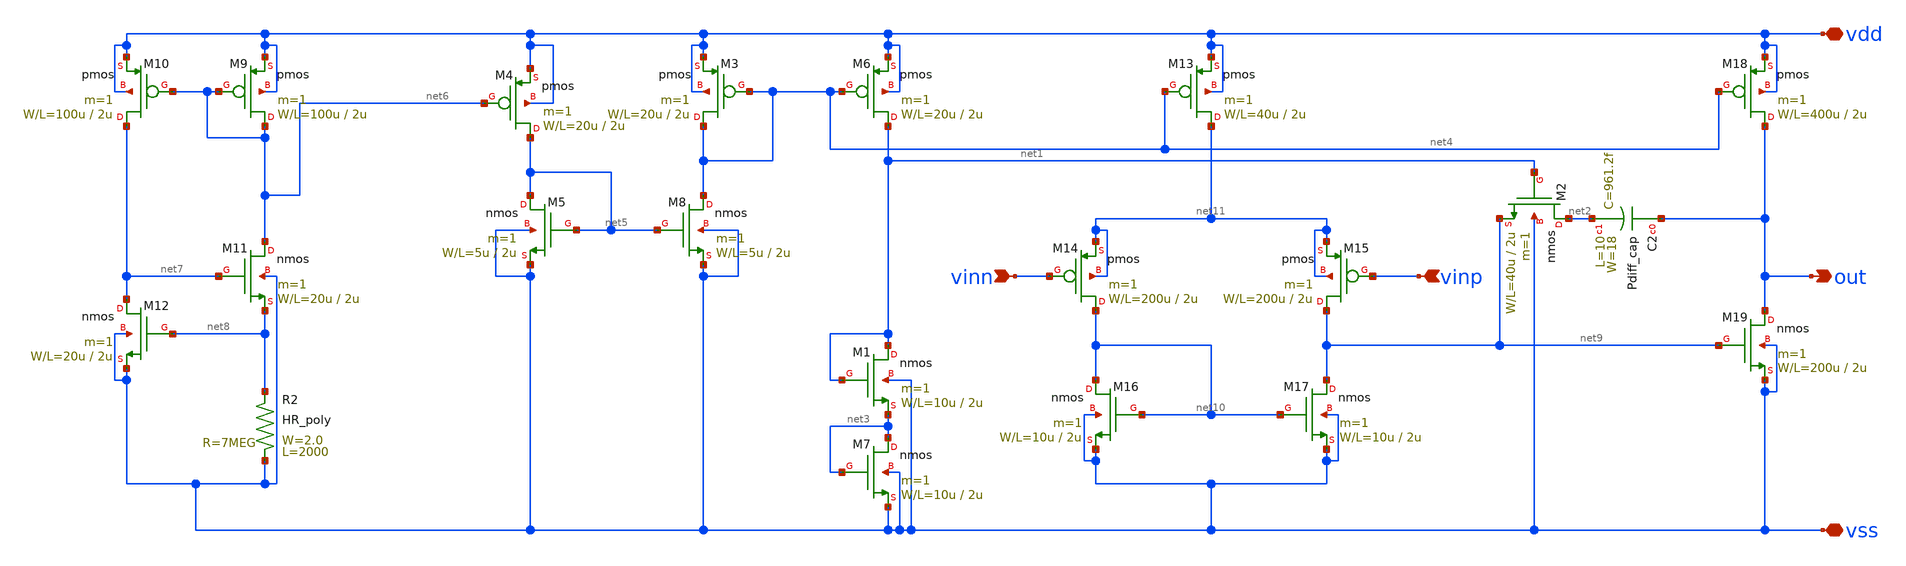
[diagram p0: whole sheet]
** sch_path: OR1/PTC06/opamp/opamp_cs_full.sch
**.subckt opamp_cs_full vdd vss vinn vinp out
*.iopin vdd
*.iopin vss
*.ipin vinn
*.ipin vinp
*.opin out
M3 net4 net4 vdd vdd pmos L=2u W=20u m=1
M2 net2 net1 net9 vss nmos L=2u W=40u m=1
M6 net1 net4 vdd vdd pmos L=2u W=20u m=1
M1 net1 net1 net3 vss nmos L=2u W=10u m=1
M7 net3 net3 vss vss nmos L=2u W=10u m=1
M4 net5 net6 vdd vdd pmos L=2u W=20u m=1
M5 net5 net5 vss vss nmos L=2u W=5u m=1
M8 net4 net5 vss vss nmos L=2u W=5u m=1
R2 vss net8 HR_poly W=2.0 L=2000
M9 net6 net6 vdd vdd pmos L=2u W=100u m=1
M10 net7 net6 vdd vdd pmos L=2u W=100u m=1
M11 net6 net7 net8 vss nmos L=2u W=20u m=1
M12 net7 net8 vss vss nmos L=2u W=20u m=1
M13 net11 net4 vdd vdd pmos L=2u W=40u m=1
M14 net10 vinn net11 net11 pmos L=2u W=200u m=1
M15 net9 vinp net11 net11 pmos L=2u W=200u m=1
M16 net10 net10 vss vss nmos L=2u W=10u m=1
M17 net9 net10 vss vss nmos L=2u W=10u m=1
M18 out net4 vdd vdd pmos L=2u W=400u m=1
M19 out net9 vss vss nmos L=2u W=200u m=1
C2 out net2 Pdiff_cap W=18 L=10
**.ends
.end
